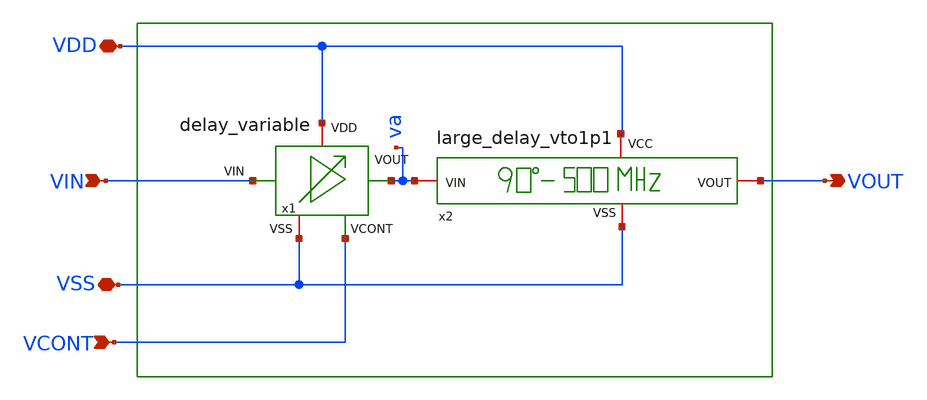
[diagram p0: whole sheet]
** sch_path: sch/delay_variable_line/variable_delay_line.sch
**.subckt variable_delay_line VSS VDD VIN VOUT VCONT
*.iopin VSS
*.iopin VDD
*.ipin VIN
*.opin VOUT
*.ipin VCONT
x1 VDD VIN va VCONT VSS delay_variable
x2 VDD VSS va VOUT large_delay_vto1p1
**.ends

* expanding   symbol:  /foss/designs/UNIC-CASS-Aug25/sch/delay_variable/delay_variable.sym # of
*+ pins=5
** sym_path: PhaseInterpolator/2to4/delay_variable.sym
** sch_path: PhaseInterpolator/2to4/delay_variable.sch
.subckt delay_variable VDD VIN VOUT VCONT VSS
*.iopin VSS
*.iopin VDD
*.opin VOUT
*.ipin VCONT
*.ipin VIN
XM1 VOUT VIN net2 VSS sg13_lv_nmos w=0.15u l=0.13u ng=1 m=4 mm_ok=1
XM2 net2 VCONT VSS VSS sg13_lv_nmos w=0.15u l=0.25u ng=1 m=2 mm_ok=1
XM3 net3 VCONT VSS VSS sg13_lv_nmos w=0.15u l=0.25u ng=1 m=1 mm_ok=1
XM5 VOUT VIN net1 VDD sg13_lv_pmos w=0.15u l=0.13u ng=1 m=4 mm_ok=1
XM6 net1 net3 VDD VDD sg13_lv_pmos w=0.15u l=0.25u ng=1 m=2 mm_ok=1
XM4 net3 net3 VDD VDD sg13_lv_pmos w=0.15u l=0.25u ng=1 m=1 mm_ok=1
.ends


* expanding   symbol:  /foss/designs/UNIC-CASS-Aug25/sch/large_delay_vto1p1/large_delay_vto1p1.sym #
*+ of pins=4
** sym_path: sch/large_delay_vto1p1/large_delay_vto1p1.sym
** sch_path: sch/large_delay_vto1p1/large_delay_vto1p1.sch
.subckt large_delay_vto1p1 VCC VSS VIN VOUT
*.iopin VIN
*.iopin VOUT
*.iopin VCC
*.iopin VSS
x1 net1 VIN VCC VSS sg13g2_dlygate4sd1_1
x2 net1 VIN VCC VSS sg13g2_dlygate4sd1_1
x3 net1 VIN VCC VSS sg13g2_dlygate4sd1_1
x4 net1 VIN VCC VSS sg13g2_dlygate4sd1_1
x5 VOUT net1 VCC VSS sg13g2_dlygate4sd3_1
.ends


* expanding   symbol:  sg13g2_stdcells/sg13g2_dlygate4sd3_1.sym # of pins=2
** sym_path: sg13g2_stdcells/sg13g2_dlygate4sd3_1.sym
** sch_path: sg13g2_stdcells/sg13g2_dlygate4sd3_1.sch
.subckt sg13g2_dlygate4sd3_1 X A VDD VSS
*.ipin A
*.opin X
*.iopin VDD
*.iopin VSS
XM1 net3 A VSS VSS sg13_lv_nmos w=420.00n l=130.00n ng=1 m=1 mm_ok=1
XM2 net1 net3 VSS VSS sg13_lv_nmos w=420.00n l=500.0n ng=1 m=1 mm_ok=1
XM3 net2 net1 VSS VSS sg13_lv_nmos w=420.00n l=500.0n ng=1 m=1 mm_ok=1
XM4 X net2 VSS VSS sg13_lv_nmos w=740.00n l=130.00n ng=1 m=1 mm_ok=1
XM5 net3 A VDD VDD sg13_lv_pmos w=420.00n l=130.00n ng=1 m=1 mm_ok=1
XM6 net1 net3 VDD VDD sg13_lv_pmos w=1.000u l=500.0n ng=1 m=1 mm_ok=1
XM7 net2 net1 VDD VDD sg13_lv_pmos w=1.000u l=500.0n ng=1 m=1 mm_ok=1
XM8 X net2 VDD VDD sg13_lv_pmos w=1.12u l=130.00n ng=1 m=1 mm_ok=1
.ends


* expanding   symbol:  sg13g2_stdcells/sg13g2_dlygate4sd1_1.sym # of pins=2
** sym_path: sg13g2_stdcells/sg13g2_dlygate4sd1_1.sym
** sch_path: sg13g2_stdcells/sg13g2_dlygate4sd1_1.sch
.subckt sg13g2_dlygate4sd1_1 X A VDD VSS
*.ipin A
*.opin X
*.iopin VDD
*.iopin VSS
XM1 net2 A VSS VSS sg13_lv_nmos w=420.00n l=130.00n ng=1 m=1 mm_ok=1
XM2 net1 net2 VSS VSS sg13_lv_nmos w=420.00n l=130.00n ng=1 m=1 mm_ok=1
XM3 net3 net1 VSS VSS sg13_lv_nmos w=420.00n l=130.00n ng=1 m=1 mm_ok=1
XM4 X net3 VSS VSS sg13_lv_nmos w=740.00n l=130.00n ng=1 m=1 mm_ok=1
XM5 net2 A VDD VDD sg13_lv_pmos w=420.00n l=130.00n ng=1 m=1 mm_ok=1
XM6 net1 net2 VDD VDD sg13_lv_pmos w=1.000u l=130.00n ng=1 m=1 mm_ok=1
XM7 net3 net1 VDD VDD sg13_lv_pmos w=1.000u l=130.00n ng=1 m=1 mm_ok=1
XM8 X net3 VDD VDD sg13_lv_pmos w=1.12u l=130.00n ng=1 m=1 mm_ok=1
.ends

.end
